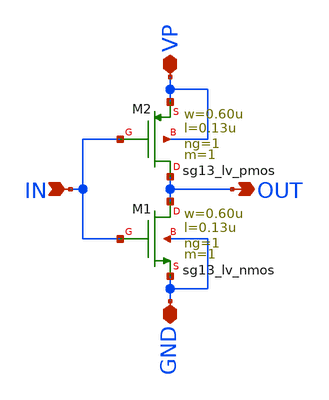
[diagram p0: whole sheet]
** sch_path: divider/inverter_x4.sch
**.subckt inverter_x4 IN VP OUT GND
*.ipin IN
*.iopin VP
*.opin OUT
*.iopin GND
XM1 OUT IN GND GND sg13_lv_nmos w=0.60u l=0.13u ng=1 m=1 mm_ok=1
XM2 OUT IN VP VP sg13_lv_pmos w=0.60u l=0.13u ng=1 m=1 mm_ok=1
**.ends
.end
